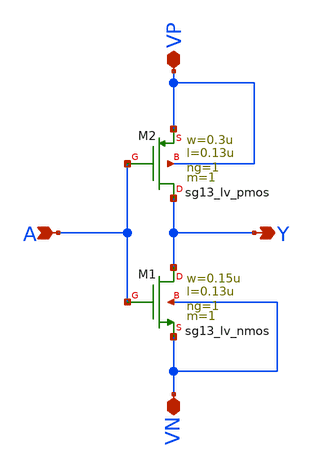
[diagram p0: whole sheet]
** sch_path: Team 2 Design/design_data/xschem/t2_inverter.sch
**.subckt t2_inverter VP VN A Y
*.iopin VP
*.iopin VN
*.ipin A
*.opin Y
XM2 Y A VP VP sg13_lv_pmos w=0.3u l=0.13u ng=1 m=1 mm_ok=1
XM1 Y A VN VN sg13_lv_nmos w=0.15u l=0.13u ng=1 m=1 mm_ok=1
**.ends
.end
